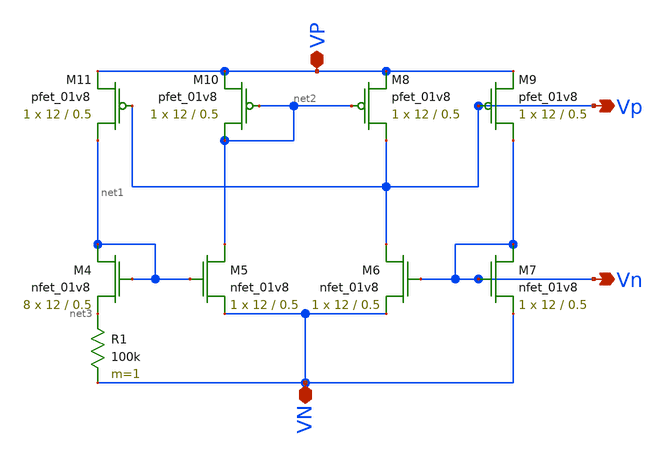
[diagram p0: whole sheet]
** sch_path: Final DAC files/current bias/current_bias.sch
**.subckt current_bias VP VN Vn Vp
*.iopin VP
*.iopin VN
*.opin Vn
*.opin Vp
XM4 net1 net1 net3 GND sky130_fd_pr__nfet_01v8 L=0.5 W=12 nf=1 ad='int((nf+1)/2) * W/nf * 0.29' as='int((nf+2)/2) * W/nf * 0.29'
+ pd='2*int((nf+1)/2) * (W/nf + 0.29)' ps='2*int((nf+2)/2) * (W/nf + 0.29)' nrd='0.29 / W' nrs='0.29 / W'
+ sa=0 sb=0 sd=0 mult=8 m=8
XM5 net2 net1 VN GND sky130_fd_pr__nfet_01v8 L=0.5 W=12 nf=1 ad='int((nf+1)/2) * W/nf * 0.29' as='int((nf+2)/2) * W/nf * 0.29'
+ pd='2*int((nf+1)/2) * (W/nf + 0.29)' ps='2*int((nf+2)/2) * (W/nf + 0.29)' nrd='0.29 / W' nrs='0.29 / W'
+ sa=0 sb=0 sd=0 mult=1 m=1
XM6 Vp Vn VN GND sky130_fd_pr__nfet_01v8 L=0.5 W=12 nf=1 ad='int((nf+1)/2) * W/nf * 0.29' as='int((nf+2)/2) * W/nf * 0.29'
+ pd='2*int((nf+1)/2) * (W/nf + 0.29)' ps='2*int((nf+2)/2) * (W/nf + 0.29)' nrd='0.29 / W' nrs='0.29 / W'
+ sa=0 sb=0 sd=0 mult=1 m=1
XM7 Vn Vn VN GND sky130_fd_pr__nfet_01v8 L=0.5 W=12 nf=1 ad='int((nf+1)/2) * W/nf * 0.29' as='int((nf+2)/2) * W/nf * 0.29'
+ pd='2*int((nf+1)/2) * (W/nf + 0.29)' ps='2*int((nf+2)/2) * (W/nf + 0.29)' nrd='0.29 / W' nrs='0.29 / W'
+ sa=0 sb=0 sd=0 mult=1 m=1
R1 net3 VN 100k m=1
XM8 Vp net2 VP VDD sky130_fd_pr__pfet_01v8 L=0.5 W=12 nf=1 ad='int((nf+1)/2) * W/nf * 0.29' as='int((nf+2)/2) * W/nf * 0.29'
+ pd='2*int((nf+1)/2) * (W/nf + 0.29)' ps='2*int((nf+2)/2) * (W/nf + 0.29)' nrd='0.29 / W' nrs='0.29 / W'
+ sa=0 sb=0 sd=0 mult=1 m=1
XM9 Vn Vp VP VDD sky130_fd_pr__pfet_01v8 L=0.5 W=12 nf=1 ad='int((nf+1)/2) * W/nf * 0.29' as='int((nf+2)/2) * W/nf * 0.29'
+ pd='2*int((nf+1)/2) * (W/nf + 0.29)' ps='2*int((nf+2)/2) * (W/nf + 0.29)' nrd='0.29 / W' nrs='0.29 / W'
+ sa=0 sb=0 sd=0 mult=1 m=1
XM10 net2 net2 VP VDD sky130_fd_pr__pfet_01v8 L=0.5 W=12 nf=1 ad='int((nf+1)/2) * W/nf * 0.29' as='int((nf+2)/2) * W/nf * 0.29'
+ pd='2*int((nf+1)/2) * (W/nf + 0.29)' ps='2*int((nf+2)/2) * (W/nf + 0.29)' nrd='0.29 / W' nrs='0.29 / W'
+ sa=0 sb=0 sd=0 mult=1 m=1
XM11 net1 Vp VP VDD sky130_fd_pr__pfet_01v8 L=0.5 W=12 nf=1 ad='int((nf+1)/2) * W/nf * 0.29' as='int((nf+2)/2) * W/nf * 0.29'
+ pd='2*int((nf+1)/2) * (W/nf + 0.29)' ps='2*int((nf+2)/2) * (W/nf + 0.29)' nrd='0.29 / W' nrs='0.29 / W'
+ sa=0 sb=0 sd=0 mult=1 m=1
**.ends
.end
